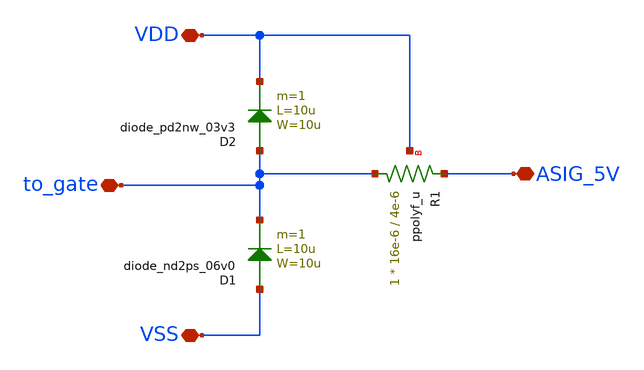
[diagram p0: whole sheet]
** sch_path: designs/libs/core_analog/ESD/io_secondary_5p0.sch
**.subckt io_secondary_5p0 VSS VDD to_gate ASIG_5V
*.iopin VSS
*.iopin VDD
*.iopin to_gate
*.iopin ASIG_5V
D1 VSS to_gate diode_nd2ps_06v0 area='10u * 10u ' pj='2*10u + 2*10u ' m=1
D2 to_gate VDD diode_pd2nw_03v3 area='10u * 10u ' pj='2*10u + 2*10u ' m=1
XR1 to_gate ASIG_5V VDD ppolyf_u r_width=16e-6 r_length=4e-6 m=1
**.ends
.end
